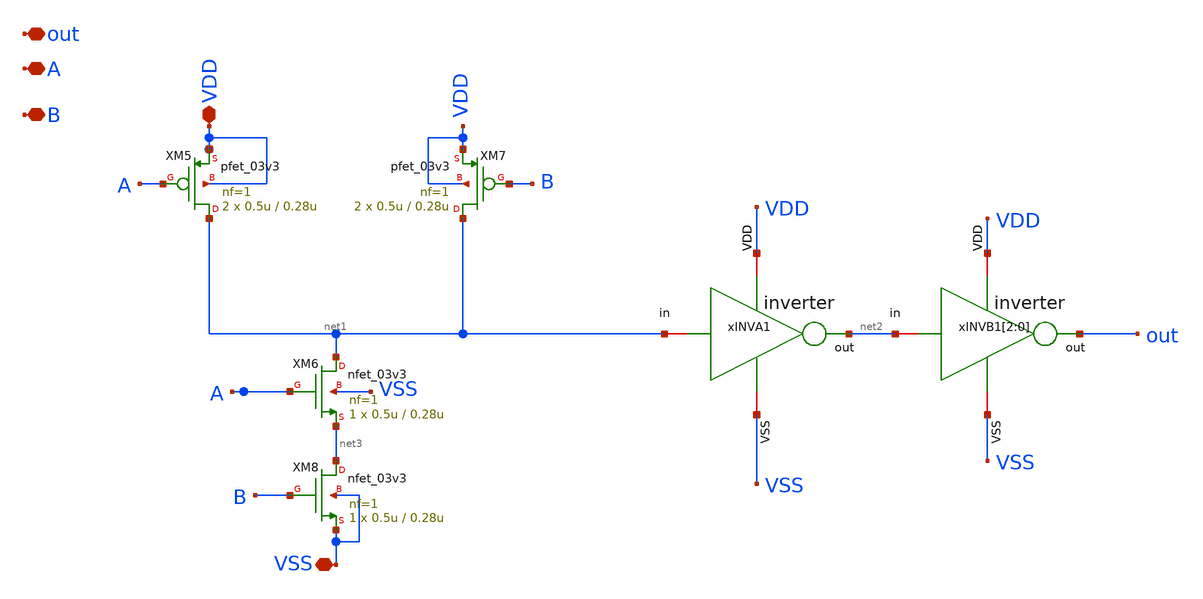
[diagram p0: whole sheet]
** sch_path: designs/sar_adc/digital/NAND/xschem/NAND.sch
**.subckt NAND A B out VDD VSS
*.iopin A
*.iopin B
*.iopin out
*.iopin VDD
*.iopin VSS
xINVA1 VDD net1 net2 VSS inverter
xINVB1[2] VDD net2 out VSS inverter
xINVB1[1] VDD net2 out VSS inverter
xINVB1[0] VDD net2 out VSS inverter
XM5 net1 A VDD VDD pfet_03v3 L=0.28u W=0.5u nf=1 ad='int((nf+1)/2) * W/nf * 0.18u' as='int((nf+2)/2) * W/nf * 0.18u'
+ pd='2*int((nf+1)/2) * (W/nf + 0.18u)' ps='2*int((nf+2)/2) * (W/nf + 0.18u)' nrd='0.18u / W' nrs='0.18u / W'
+ sa=0 sb=0 sd=0 m=2
XM6 net1 A net3 VSS nfet_03v3 L=0.28u W=0.5u nf=1 ad='int((nf+1)/2) * W/nf * 0.18u' as='int((nf+2)/2) * W/nf * 0.18u'
+ pd='2*int((nf+1)/2) * (W/nf + 0.18u)' ps='2*int((nf+2)/2) * (W/nf + 0.18u)' nrd='0.18u / W' nrs='0.18u / W'
+ sa=0 sb=0 sd=0 m=1
XM7 net1 B VDD VDD pfet_03v3 L=0.28u W=0.5u nf=1 ad='int((nf+1)/2) * W/nf * 0.18u' as='int((nf+2)/2) * W/nf * 0.18u'
+ pd='2*int((nf+1)/2) * (W/nf + 0.18u)' ps='2*int((nf+2)/2) * (W/nf + 0.18u)' nrd='0.18u / W' nrs='0.18u / W'
+ sa=0 sb=0 sd=0 m=2
XM8 net3 B VSS VSS nfet_03v3 L=0.28u W=0.5u nf=1 ad='int((nf+1)/2) * W/nf * 0.18u' as='int((nf+2)/2) * W/nf * 0.18u'
+ pd='2*int((nf+1)/2) * (W/nf + 0.18u)' ps='2*int((nf+2)/2) * (W/nf + 0.18u)' nrd='0.18u / W' nrs='0.18u / W'
+ sa=0 sb=0 sd=0 m=1
**.ends

* expanding   symbol:  designs/sar_adc/digital/inverter/xschem/inverter.sym # of pins=6
** sym_path: designs/sar_adc/digital/inverter/xschem/inverter.sym
** sch_path: designs/sar_adc/digital/inverter/xschem/inverter.sch
.subckt inverter VDD in out VSS
*.opin out
*.iopin in
*.iopin VDD
*.iopin VSS
XM1 out in VSS VSS nfet_03v3 L=0.28u W=1u nf=1 ad='int((nf+1)/2) * W/nf * 0.18u' as='int((nf+2)/2) * W/nf * 0.18u'
+ pd='2*int((nf+1)/2) * (W/nf + 0.18u)' ps='2*int((nf+2)/2) * (W/nf + 0.18u)' nrd='0.18u / W' nrs='0.18u / W'
+ sa=0 sb=0 sd=0 m=1
XM2 out in VDD VDD pfet_03v3 L=0.28u W=3u nf=1 ad='int((nf+1)/2) * W/nf * 0.18u' as='int((nf+2)/2) * W/nf * 0.18u'
+ pd='2*int((nf+1)/2) * (W/nf + 0.18u)' ps='2*int((nf+2)/2) * (W/nf + 0.18u)' nrd='0.18u / W' nrs='0.18u / W'
+ sa=0 sb=0 sd=0 m=1
.ends

.end
